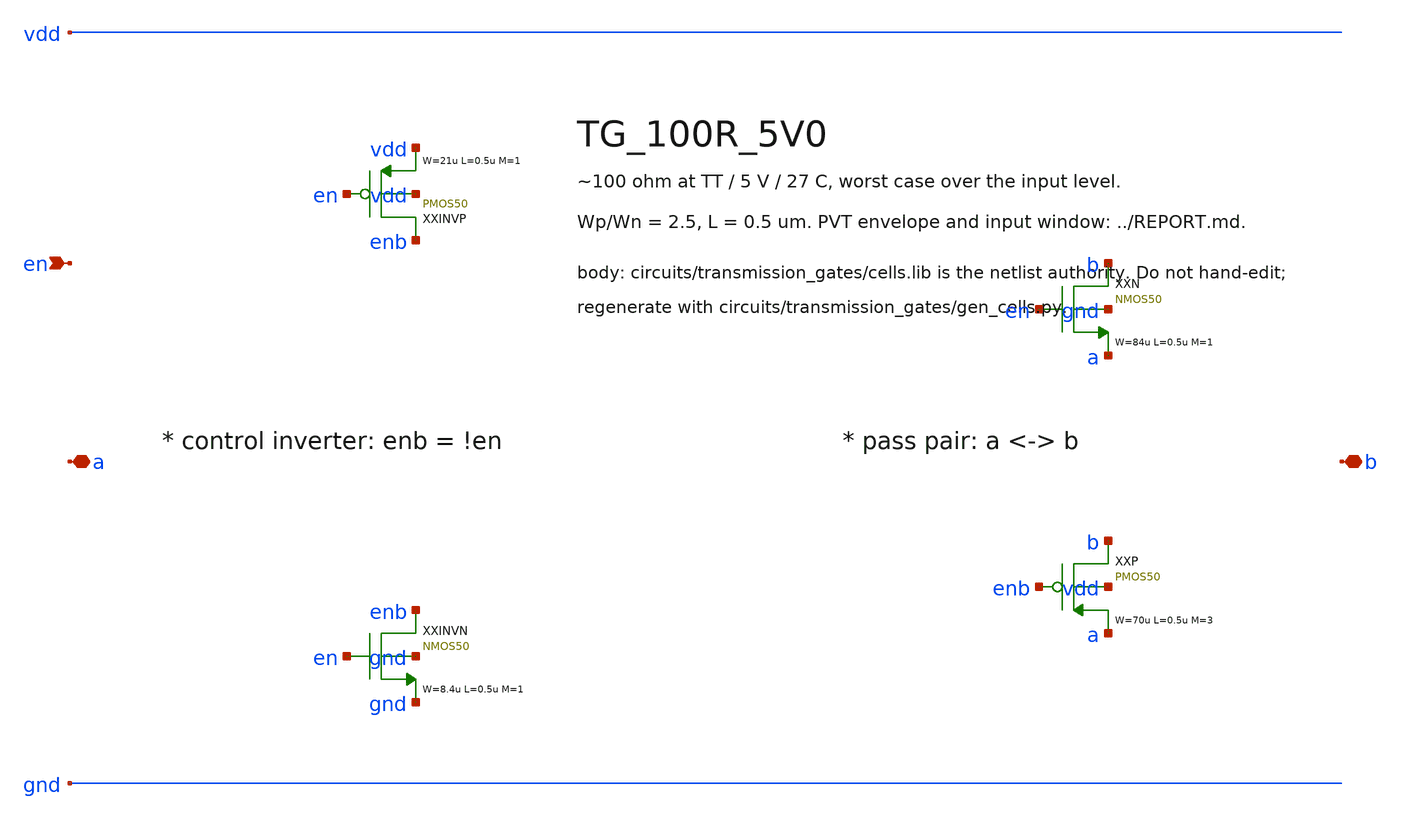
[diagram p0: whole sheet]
** sch_path: xschem/transmission_gates/TG_100R_5V0.sch
**.subckt TG_100R_5V0 a b en
*.iopin a
*.iopin b
*.ipin en
XXINVP enb en vdd vdd PMOS50 W=21u L=0.5u M=1 MM_SIGMA=0
XXINVN enb en gnd gnd NMOS50 W=8.4u L=0.5u M=1 MM_SIGMA=0
XXN b en a gnd NMOS50 W=84u L=0.5u M=1 MM_SIGMA=0
XXP b enb a vdd PMOS50 W=70u L=0.5u M=3 MM_SIGMA=0
**.ends
.end
